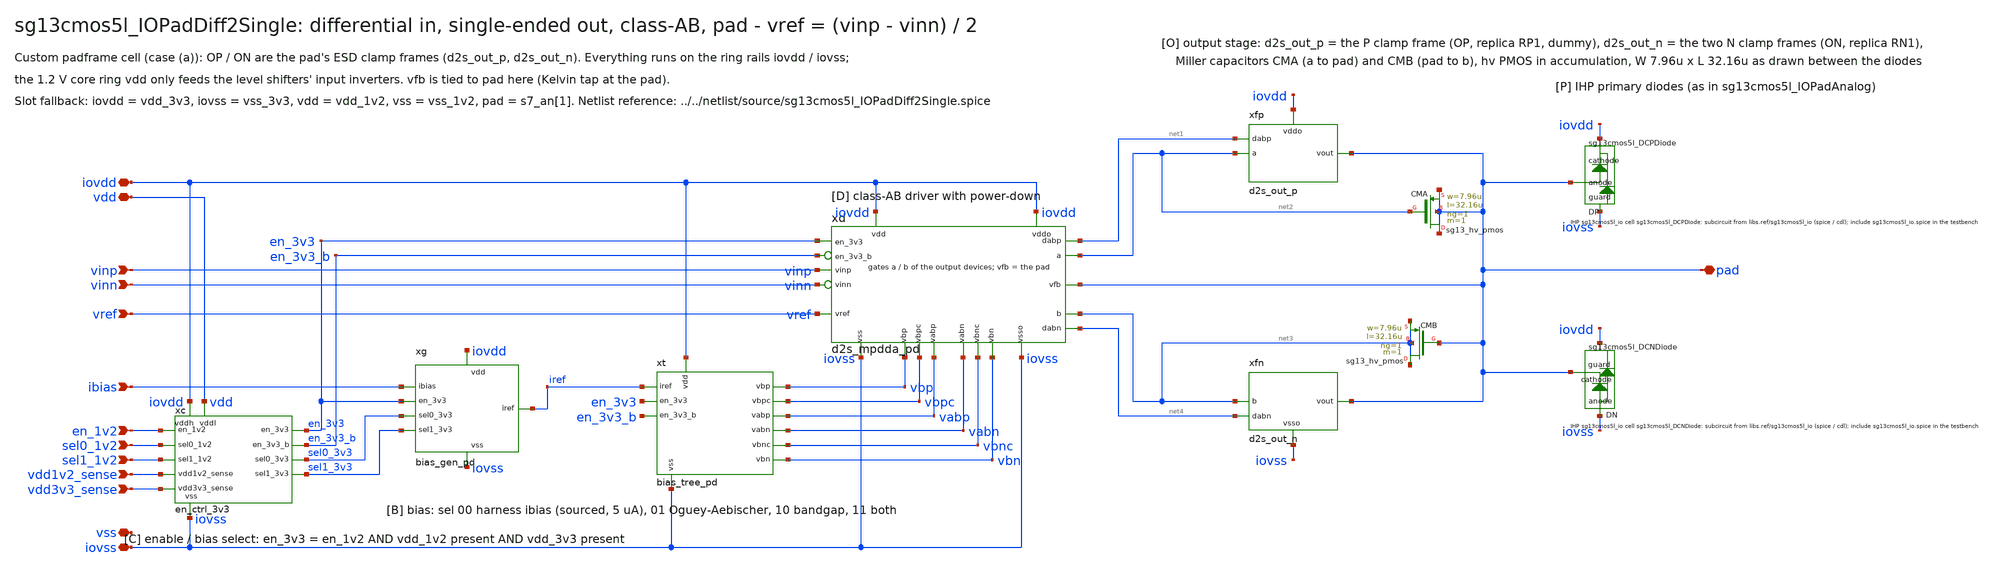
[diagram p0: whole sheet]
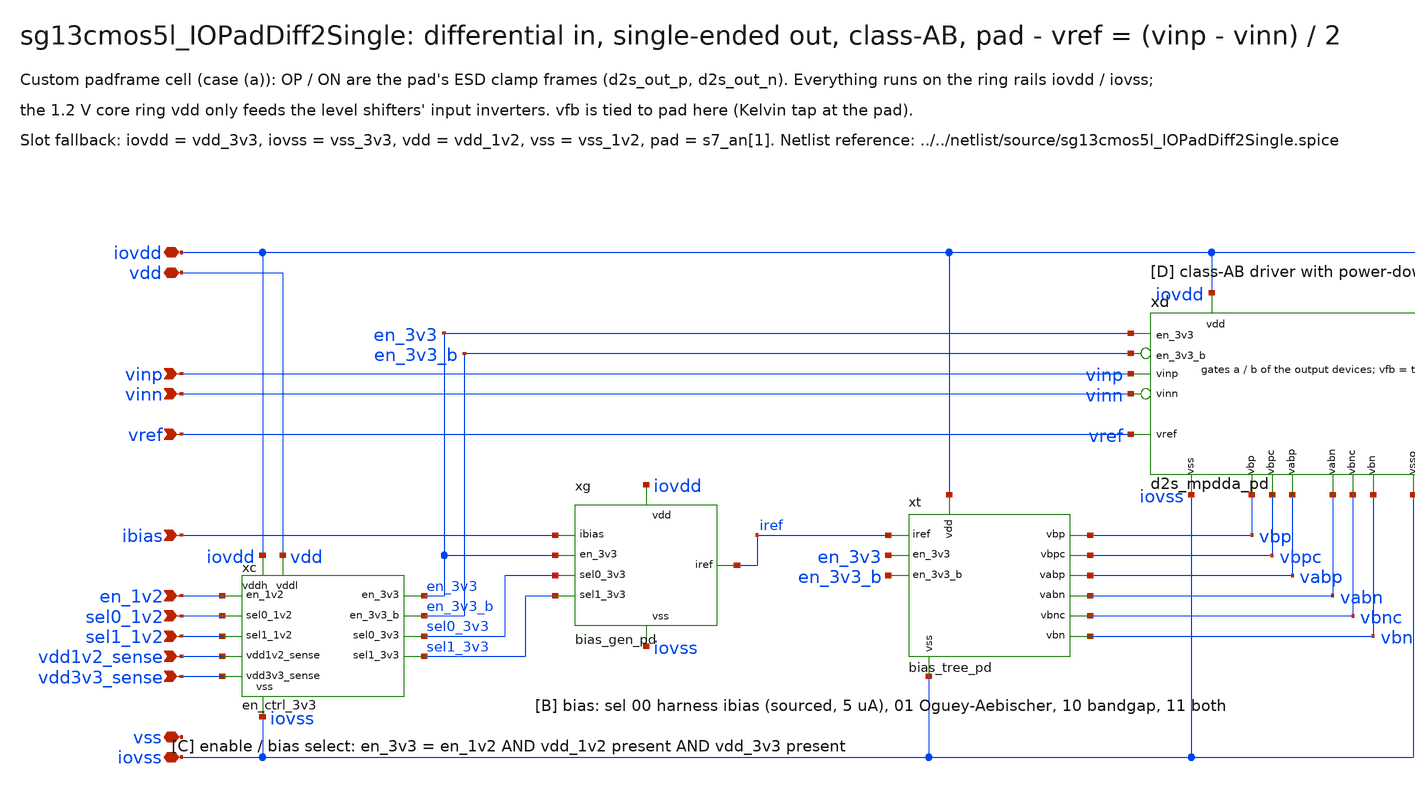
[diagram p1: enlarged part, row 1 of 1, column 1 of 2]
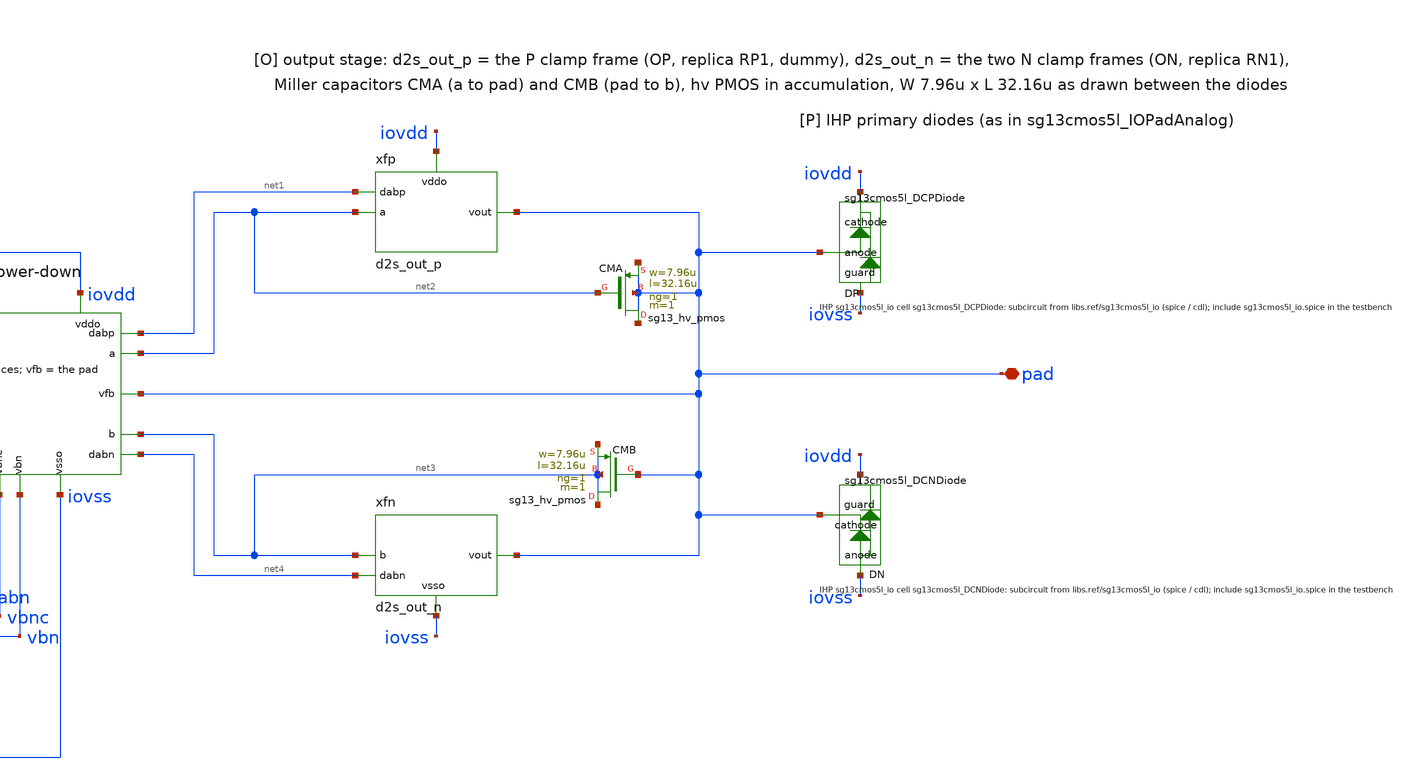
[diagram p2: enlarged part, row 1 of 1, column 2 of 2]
** sch_path: sudelbuecher/design_considerations/pad_buffer_layout/pad_cell_2026-10-31/macro_before/macros/sg13cmos5l_IOPadDiff2Single/schematic/xschem/sg13cmos5l_IOPadDiff2Single.sch
**.subckt sg13cmos5l_IOPadDiff2Single iovdd iovss vdd vss vinp vinn vref ibias en_1v2 sel0_1v2
*+ sel1_1v2 vdd1v2_sense vdd3v3_sense pad
*.iopin iovdd
*.iopin iovss
*.iopin vdd
*.iopin vss
*.ipin vinp
*.ipin vinn
*.ipin vref
*.ipin ibias
*.ipin en_1v2
*.ipin sel0_1v2
*.ipin sel1_1v2
*.ipin vdd1v2_sense
*.ipin vdd3v3_sense
*.iopin pad
xc iovdd vdd iovss en_1v2 sel0_1v2 sel1_1v2 vdd1v2_sense vdd3v3_sense en_3v3 sel0_3v3 sel1_3v3
+ en_3v3_b en_ctrl_3v3
xd iovdd iovss iovdd iovss vinp vinn vref pad net2 net3 net1 net4 vbp vbn vbpc vbnc vabp vabn en_3v3
+ en_3v3_b d2s_mpdda_pd
xfp iovdd net2 pad net1 d2s_out_p
xfn iovss net3 pad net4 d2s_out_n
XCMA pad net2 pad pad sg13_hv_pmos w=7.96u l=32.16u ng=1 m=1 mm_ok=1
XCMB net3 pad net3 net3 sg13_hv_pmos w=7.96u l=32.16u ng=1 m=1 mm_ok=1
XDP pad iovdd iovss sg13cmos5l_DCPDiode
XDN iovss pad iovdd sg13cmos5l_DCNDiode
xg iovdd iovss ibias iref en_3v3 sel0_3v3 sel1_3v3 bias_gen_pd
xt iovdd iovss iref vbp vbn vbpc vbnc vabp vabn en_3v3 en_3v3_b bias_tree_pd
**.ends
.end
